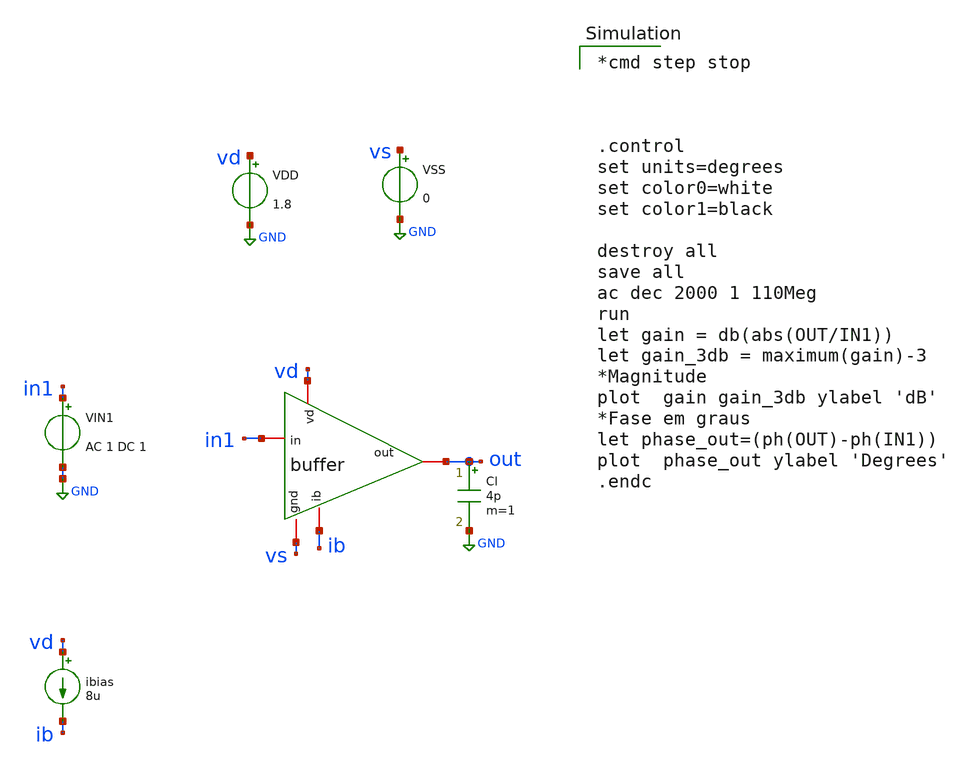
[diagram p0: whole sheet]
** sch_path: buffer/xschem/buffer_tb-ac.sch
* Copyright 2020 Stefan Frederik Schippers
* Licensed under the Apache License, Version 2.0 (the "License");
* you may not use this file except in compliance with the License.
* You may obtain a copy of the License at
* https://www.apache.org/licenses/LICENSE-2.0
* Unless required by applicable law or agreed to in writing, software
* distributed under the License is distributed on an "AS IS" BASIS,
* WITHOUT WARRANTIES OR CONDITIONS OF ANY KIND, either express or implied.
* See the License for the specific language governing permissions and
* limitations under the License.
**.subckt buffer_tb-ac
VIN1 in1 GND AC 1 DC 1
ibias vd ib 8u
VDD vd GND 1.8
VSS vs GND 0
Cl out GND 4p m=1
X1 vd in1 out ib vs buffer
**** begin user architecture code

*cmd step stop



.control
set units=degrees
set color0=white
set color1=black

destroy all
save all
ac dec 2000 1 110Meg
run
let gain = db(abs(OUT/IN1))
let gain_3db = maximum(gain)-3
*Magnitude
plot  gain gain_3db ylabel 'dB'
*Fase em graus
let phase_out=(ph(OUT)-ph(IN1))
plot  phase_out ylabel 'Degrees'
.endc

 .lib $::SKYWATER_MODELS/sky130.lib.spice tt
.include $::SKYWATER_STDCELLS/sky130_fd_sc_hd.spice

**** end user architecture code
**.ends

* expanding   symbol:  /home/hugodg/projects-sky130/temp-sensor/buffer/xschem/buffer.sym # of pins=5
** sym_path: buffer/xschem/buffer.sym
** sch_path: buffer/xschem/buffer.sch
.subckt buffer vd in out ib gnd
*.iopin vd
*.iopin ib
*.iopin out
*.iopin in
*.iopin gnd
XM3 net2 net2 vd vd sky130_fd_pr__pfet_01v8 L=1 W=1 nf=1 ad='int((nf+1)/2) * W/nf * 0.29' as='int((nf+2)/2) * W/nf * 0.29'
+ pd='2*int((nf+1)/2) * (W/nf + 0.29)' ps='2*int((nf+2)/2) * (W/nf + 0.29)' nrd='0.29 / W' nrs='0.29 / W'
+ sa=0 sb=0 sd=0 mult=1 m=1
XM1 net2 out net4 gnd sky130_fd_pr__nfet_01v8 L=1 W=10 nf=10 ad='int((nf+1)/2) * W/nf * 0.29' as='int((nf+2)/2) * W/nf * 0.29'
+ pd='2*int((nf+1)/2) * (W/nf + 0.29)' ps='2*int((nf+2)/2) * (W/nf + 0.29)' nrd='0.29 / W' nrs='0.29 / W'
+ sa=0 sb=0 sd=0 mult=1 m=1
XM2 net3 in net4 gnd sky130_fd_pr__nfet_01v8 L=1 W=10 nf=10 ad='int((nf+1)/2) * W/nf * 0.29' as='int((nf+2)/2) * W/nf * 0.29'
+ pd='2*int((nf+1)/2) * (W/nf + 0.29)' ps='2*int((nf+2)/2) * (W/nf + 0.29)' nrd='0.29 / W' nrs='0.29 / W'
+ sa=0 sb=0 sd=0 mult=1 m=1
XM4 net3 net3 vd vd sky130_fd_pr__pfet_01v8 L=1 W=1 nf=1 ad='int((nf+1)/2) * W/nf * 0.29' as='int((nf+2)/2) * W/nf * 0.29'
+ pd='2*int((nf+1)/2) * (W/nf + 0.29)' ps='2*int((nf+2)/2) * (W/nf + 0.29)' nrd='0.29 / W' nrs='0.29 / W'
+ sa=0 sb=0 sd=0 mult=1 m=1
XM5 net4 ib gnd gnd sky130_fd_pr__nfet_01v8 L=1 W=1 nf=1 ad='int((nf+1)/2) * W/nf * 0.29' as='int((nf+2)/2) * W/nf * 0.29'
+ pd='2*int((nf+1)/2) * (W/nf + 0.29)' ps='2*int((nf+2)/2) * (W/nf + 0.29)' nrd='0.29 / W' nrs='0.29 / W'
+ sa=0 sb=0 sd=0 mult=1 m=1
XM6 out net3 vd vd sky130_fd_pr__pfet_01v8 L=1 W=10 nf=10 ad='int((nf+1)/2) * W/nf * 0.29' as='int((nf+2)/2) * W/nf * 0.29'
+ pd='2*int((nf+1)/2) * (W/nf + 0.29)' ps='2*int((nf+2)/2) * (W/nf + 0.29)' nrd='0.29 / W' nrs='0.29 / W'
+ sa=0 sb=0 sd=0 mult=1 m=1
XM7 out net1 gnd gnd sky130_fd_pr__nfet_01v8 L=1 W=10 nf=10 ad='int((nf+1)/2) * W/nf * 0.29' as='int((nf+2)/2) * W/nf * 0.29'
+ pd='2*int((nf+1)/2) * (W/nf + 0.29)' ps='2*int((nf+2)/2) * (W/nf + 0.29)' nrd='0.29 / W' nrs='0.29 / W'
+ sa=0 sb=0 sd=0 mult=1 m=1
XM8 net1 net2 vd vd sky130_fd_pr__pfet_01v8 L=1 W=10 nf=10 ad='int((nf+1)/2) * W/nf * 0.29' as='int((nf+2)/2) * W/nf * 0.29'
+ pd='2*int((nf+1)/2) * (W/nf + 0.29)' ps='2*int((nf+2)/2) * (W/nf + 0.29)' nrd='0.29 / W' nrs='0.29 / W'
+ sa=0 sb=0 sd=0 mult=1 m=1
XM9 net1 net1 gnd gnd sky130_fd_pr__nfet_01v8 L=1 W=10 nf=10 ad='int((nf+1)/2) * W/nf * 0.29' as='int((nf+2)/2) * W/nf * 0.29'
+ pd='2*int((nf+1)/2) * (W/nf + 0.29)' ps='2*int((nf+2)/2) * (W/nf + 0.29)' nrd='0.29 / W' nrs='0.29 / W'
+ sa=0 sb=0 sd=0 mult=1 m=1
XM10 ib ib gnd gnd sky130_fd_pr__nfet_01v8 L=1 W=1 nf=1 ad='int((nf+1)/2) * W/nf * 0.29' as='int((nf+2)/2) * W/nf * 0.29'
+ pd='2*int((nf+1)/2) * (W/nf + 0.29)' ps='2*int((nf+2)/2) * (W/nf + 0.29)' nrd='0.29 / W' nrs='0.29 / W'
+ sa=0 sb=0 sd=0 mult=1 m=1
**** begin user architecture code


R0 in.n1 in.n0 150.875
R1 in.n5 in.n4 150.49
R2 in.n3 in.n2 150.488
R3 in.n7 in.n6 141.16
R4 in.n0 in.t9 25.228
R5 in.n6 in.t7 24.105
R6 in.n0 in.t2 24.104
R7 in.n2 in.t4 24.103
R8 in.n4 in.t0 24.102
R9 in.n1 in.t5 24.102
R10 in.n5 in.t8 24.102
R11 in.n3 in.t6 24.102
R12 in.n7 in.t3 24.102
R13 in.n9 in.t1 24.1
R14 in.n14 in.n13 9.3
R15 in in.n14 8.355
R16 in.n8 in.n7 1.785
R17 in.n2 in.n1 1.103
R18 in.n4 in.n3 1.094
R19 in.n6 in.n5 0.41
R20 in.n14 in.n12 0.076
R21 in.n12 in.n8 0.014
R22 in.n12 in.n11 0.005
R23 in.n10 in.n9 0.005
R24 in.n11 in.n10 0.001
R25 out.t0 out.n7 175.091
R26 out.n0 out.t2 175.044
R27 out.n2 out.n1 150.491
R28 out.n4 out.n3 150.491
R29 out.n6 out.n5 141.106
R30 out out.t0 28.796
R31 out.n5 out.t1 24.103
R32 out.n6 out.t7 24.103
R33 out.n4 out.t5 24.103
R34 out.n2 out.t3 24.102
R35 out.n0 out.t6 24.102
R36 out.n1 out.t9 24.102
R37 out.n3 out.t4 24.102
R38 out.n7 out.t8 24.102
R39 out.n7 out.n6 1.085
R40 out.n3 out.n2 0.988
R41 out.n5 out.n4 0.913
R42 out.n1 out.n0 0.863
R43 vd.n53 vd.n52 379.482
R44 vd.n40 vd.n34 379.482
R45 vd.n54 vd.n53 297.411
R46 vd.n41 vd.n40 297.411
R47 vd.n19 vd.n16 131.387
R48 vd.n4 vd.n1 131.387
R49 vd.n24 vd.n21 131.011
R50 vd.n9 vd.n6 131.011
R51 vd.n29 vd.n24 54.211
R52 vd.n14 vd.n9 54.211
R53 vd.n29 vd.n19 53.835
R54 vd.n14 vd.n4 53.835
R55 vd.n57 vd.n14 8.271
R56 vd.n57 vd.n29 7.938
R57 vd.n57 vd.n56 4.028
R58 vd vd.n57 1.201
R59 vd.n55 vd.n45 0.296
R60 vd.n42 vd.n32 0.228
R61 vd.n56 vd.n55 0.18
R62 vd.n56 vd.n42 0.167
R63 vd.n19 vd.n18 0.161
R64 vd.n24 vd.n23 0.161
R65 vd.n4 vd.n3 0.161
R66 vd.n9 vd.n8 0.161
R67 vd.n23 vd.n22 0.139
R68 vd.n8 vd.n7 0.139
R69 vd.n18 vd.n17 0.139
R70 vd.n3 vd.n2 0.139
R71 vd.n42 vd.n41 0.017
R72 vd.n55 vd.n54 0.017
R73 vd.n16 vd.n15 0.015
R74 vd.n21 vd.n20 0.015
R75 vd.n1 vd.n0 0.015
R76 vd.n6 vd.n5 0.015
R77 vd.n52 vd.n51 0.013
R78 vd.n34 vd.n33 0.013
R79 vd.n26 vd.n25 0.013
R80 vd.n27 vd.n26 0.013
R81 vd.n11 vd.n10 0.013
R82 vd.n12 vd.n11 0.013
R83 vd.n53 vd.n50 0.003
R84 vd.n47 vd.n46 0.003
R85 vd.n36 vd.n35 0.003
R86 vd.n40 vd.n39 0.003
R87 vd.n50 vd.n49 0.003
R88 vd.n37 vd.n36 0.003
R89 vd.n48 vd.n47 0.003
R90 vd.n39 vd.n38 0.003
R91 vd.n49 vd.n48 0.002
R92 vd.n38 vd.n37 0.002
R93 vd.n29 vd.n28 0.002
R94 vd.n28 vd.n27 0.002
R95 vd.n14 vd.n13 0.002
R96 vd.n13 vd.n12 0.002
R97 vd.n32 vd.n31 0.001
R98 vd.n45 vd.n44 0.001
R99 vd.n44 vd.n43 0.001
R100 vd.n31 vd.n30 0.001
R101 ib.n0 ib.t2 24.837
R102 ib.n0 ib.t0 24.107
R103 ib.n1 ib.t1 17.747
R104 ib ib.n1 4.155
R105 ib.n1 ib.n0 0.387
C0 net3 net4 2.13fF
C1 in net2 1.15fF
C2 out net3 3.71fF
C3 out net4 4.05fF
C4 vd net2 4.02fF
C5 net1 net2 3.05fF
C6 ib net4 0.05fF
C7 in net3 1.75fF
C8 in net4 3.76fF
C9 vd net3 4.13fF
C10 net1 net3 0.21fF
C11 out in 2.79fF
C12 net1 net4 0.05fF
C13 out vd 1.60fF
C14 in ib 0.09fF
C15 out net1 1.73fF
C16 in vd 0.31fF
C17 net3 net2 0.42fF
C18 in net1 0.33fF
C19 net2 net4 1.84fF
C20 net1 vd 2.57fF
C21 out net2 2.47fF
C22 ib.t1 gnd 0.02fF
C23 ib.t2 gnd 0.45fF
C24 ib.t0 gnd 0.44fF
C25 ib.n0 gnd 0.61fF $ **FLOATING
C26 ib.n1 gnd 0.39fF $ **FLOATING
C27 vd.n0 gnd 0.28fF $ **FLOATING
C28 vd.n1 gnd 0.05fF $ **FLOATING
C29 vd.n2 gnd 0.27fF $ **FLOATING
C30 vd.n3 gnd 0.03fF $ **FLOATING
C31 vd.n4 gnd 0.03fF $ **FLOATING
C32 vd.n5 gnd 0.28fF $ **FLOATING
C33 vd.n6 gnd 0.05fF $ **FLOATING
C34 vd.n7 gnd 0.27fF $ **FLOATING
C35 vd.n8 gnd 0.03fF $ **FLOATING
C36 vd.n9 gnd 0.03fF $ **FLOATING
C37 vd.n10 gnd 0.06fF $ **FLOATING
C38 vd.n11 gnd 0.06fF $ **FLOATING
C39 vd.n12 gnd 0.29fF $ **FLOATING
C40 vd.n13 gnd 0.02fF $ **FLOATING
C41 vd.n14 gnd 0.40fF $ **FLOATING
C42 vd.n15 gnd 0.28fF $ **FLOATING
C43 vd.n16 gnd 0.05fF $ **FLOATING
C44 vd.n17 gnd 0.27fF $ **FLOATING
C45 vd.n18 gnd 0.03fF $ **FLOATING
C46 vd.n19 gnd 0.03fF $ **FLOATING
C47 vd.n20 gnd 0.28fF $ **FLOATING
C48 vd.n21 gnd 0.05fF $ **FLOATING
C49 vd.n22 gnd 0.27fF $ **FLOATING
C50 vd.n23 gnd 0.03fF $ **FLOATING
C51 vd.n24 gnd 0.03fF $ **FLOATING
C52 vd.n25 gnd 0.06fF $ **FLOATING
C53 vd.n26 gnd 0.06fF $ **FLOATING
C54 vd.n27 gnd 0.29fF $ **FLOATING
C55 vd.n28 gnd 0.02fF $ **FLOATING
C56 vd.n29 gnd 0.42fF $ **FLOATING
C57 vd.n30 gnd 1.06fF $ **FLOATING
C58 vd.n31 gnd 0.03fF $ **FLOATING
C59 vd.n32 gnd 0.52fF $ **FLOATING
C60 vd.n33 gnd 1.06fF $ **FLOATING
C61 vd.n34 gnd 0.12fF $ **FLOATING
C62 vd.n35 gnd 0.10fF $ **FLOATING
C63 vd.n36 gnd 0.12fF $ **FLOATING
C64 vd.n37 gnd 0.82fF $ **FLOATING
C65 vd.n38 gnd 0.82fF $ **FLOATING
C66 vd.n39 gnd 0.12fF $ **FLOATING
C67 vd.n40 gnd 0.10fF $ **FLOATING
C68 vd.n41 gnd 0.06fF $ **FLOATING
C69 vd.n42 gnd 0.08fF $ **FLOATING
C70 vd.n43 gnd 1.06fF $ **FLOATING
C71 vd.n44 gnd 0.03fF $ **FLOATING
C72 vd.n45 gnd 0.28fF $ **FLOATING
C73 vd.n46 gnd 0.10fF $ **FLOATING
C74 vd.n47 gnd 0.12fF $ **FLOATING
C75 vd.n48 gnd 0.82fF $ **FLOATING
C76 vd.n49 gnd 0.82fF $ **FLOATING
C77 vd.n50 gnd 0.12fF $ **FLOATING
C78 vd.n51 gnd 1.06fF $ **FLOATING
C79 vd.n52 gnd 0.12fF $ **FLOATING
C80 vd.n53 gnd 0.10fF $ **FLOATING
C81 vd.n54 gnd 0.06fF $ **FLOATING
C82 vd.n55 gnd 0.29fF $ **FLOATING
C83 vd.n56 gnd 1.16fF $ **FLOATING
C84 vd.n57 gnd 10.99fF $ **FLOATING
C85 out.t8 gnd 0.52fF
C86 out.t1 gnd 0.52fF
C87 out.t4 gnd 0.52fF
C88 out.t9 gnd 0.52fF
C89 out.t2 gnd 0.82fF
C90 out.t6 gnd 0.52fF
C91 out.n0 gnd 2.36fF $ **FLOATING
C92 out.n1 gnd 2.48fF $ **FLOATING
C93 out.t3 gnd 0.52fF
C94 out.n2 gnd 0.76fF $ **FLOATING
C95 out.n3 gnd 0.75fF $ **FLOATING
C96 out.t5 gnd 0.52fF
C97 out.n4 gnd 0.80fF $ **FLOATING
C98 out.n5 gnd 0.81fF $ **FLOATING
C99 out.t7 gnd 0.52fF
C100 out.n6 gnd 0.74fF $ **FLOATING
C101 out.n7 gnd 0.80fF $ **FLOATING
C102 out.t0 gnd 0.79fF
C103 in.t0 gnd 0.54fF
C104 in.t5 gnd 0.54fF
C105 in.t9 gnd 0.57fF
C106 in.t2 gnd 0.54fF
C107 in.n0 gnd 1.47fF $ **FLOATING
C108 in.n1 gnd 0.76fF $ **FLOATING
C109 in.t4 gnd 0.54fF
C110 in.n2 gnd 0.76fF $ **FLOATING
C111 in.t6 gnd 0.54fF
C112 in.n3 gnd 0.76fF $ **FLOATING
C113 in.n4 gnd 0.76fF $ **FLOATING
C114 in.t8 gnd 0.54fF
C115 in.n5 gnd 0.90fF $ **FLOATING
C116 in.t7 gnd 0.54fF
C117 in.n6 gnd 0.90fF $ **FLOATING
C118 in.t3 gnd 0.54fF
C119 in.n7 gnd 0.64fF $ **FLOATING
C120 in.n8 gnd 0.28fF $ **FLOATING
C121 in.t1 gnd 0.54fF
C122 in.n9 gnd 0.23fF $ **FLOATING
C123 in.n11 gnd 0.01fF $ **FLOATING
C124 in.n12 gnd 0.02fF $ **FLOATING
C125 in.n13 gnd 0.03fF $ **FLOATING
C126 in.n14 gnd 0.50fF $ **FLOATING
C127 net4 gnd -1.92fF
C128 ib gnd 2.35fF
C129 out gnd 3.80fF
C130 net3 gnd -0.61fF
C131 vd gnd -15.82fF
C132 net1 gnd 16.37fF
C133 net2 gnd 2.13fF
C134 in gnd 4.77fF


**** end user architecture code
.ends

.GLOBAL GND
.end
